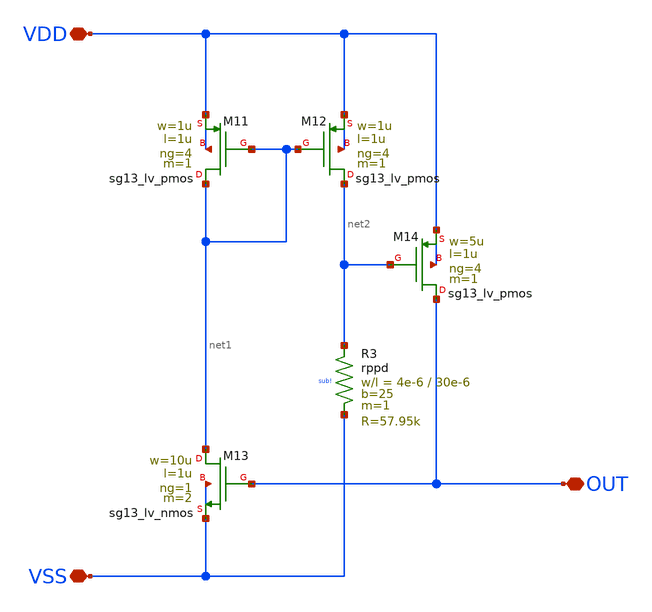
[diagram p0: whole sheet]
** sch_path: 10_xschem/startup_circuit.sch
**.subckt startup_circuit VDD VSS OUT
*.iopin VDD
*.iopin VSS
*.iopin OUT
XM11 net1 net1 VDD VDD sg13_lv_pmos w=1u l=1u ng=4 m=1 mm_ok=1
XM12 net2 net1 VDD VDD sg13_lv_pmos w=1u l=1u ng=4 m=1 mm_ok=1
XM13 net1 OUT VSS VSS sg13_lv_nmos w=10u l=1u ng=1 m=2 mm_ok=1
XR3 net2 VSS sub! rppd w=4e-6 l=30e-6 m=1 b=25 mm_ok=1
XM14 OUT net2 VDD VDD sg13_lv_pmos w=5u l=1u ng=4 m=1 mm_ok=1
**.ends
.end
